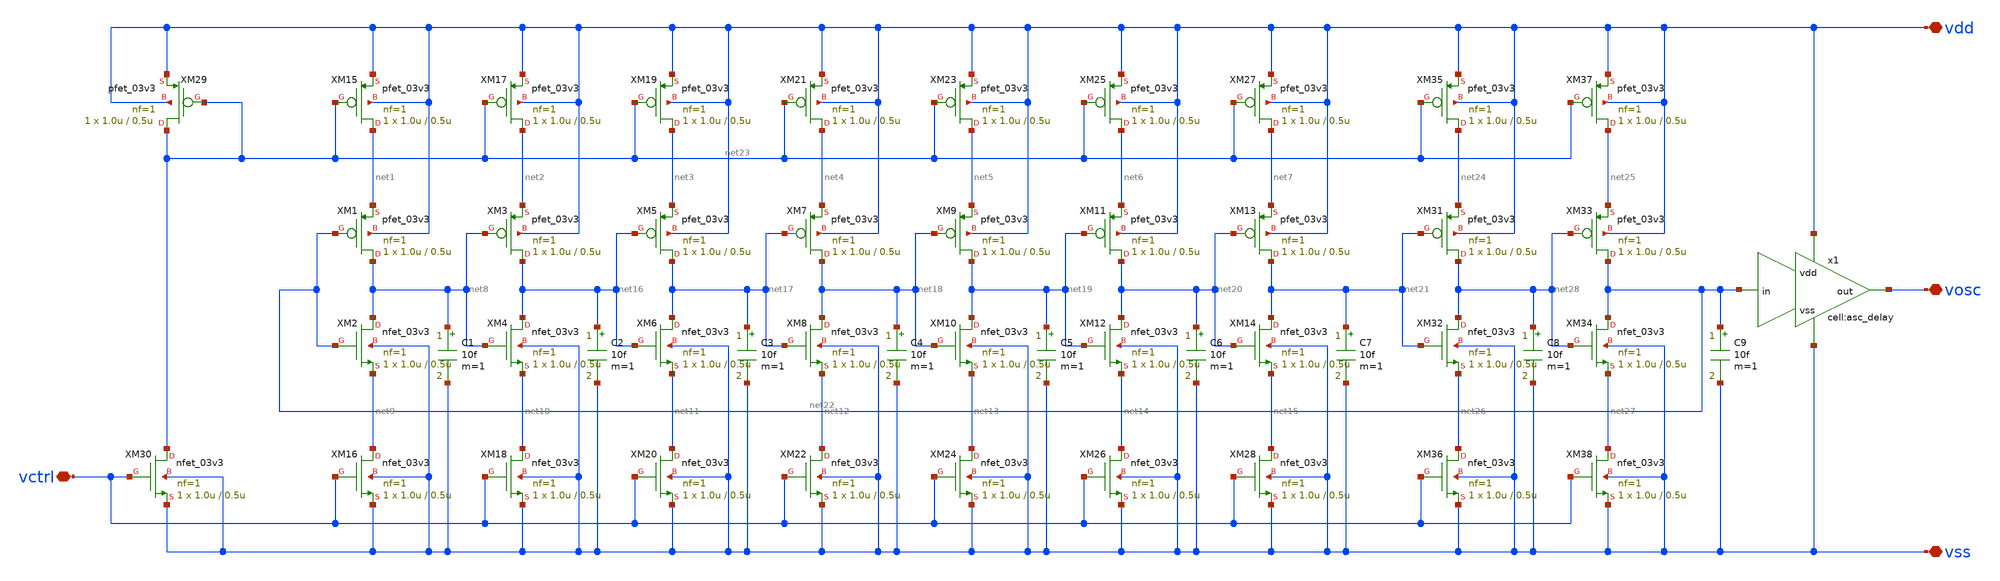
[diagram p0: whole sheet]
** sch_path: designs/libs/core_analog/CSRVCO_20250818/CSRVCO_20250818.sch
**.subckt CSRVCO_20250818 vdd vss vosc vctrl
*.iopin vdd
*.iopin vss
*.iopin vosc
*.iopin vctrl
XM1 net8 net22 net1 vdd pfet_03v3 L=0.5u W=1.0u nf=1 ad='int((nf+1)/2) * W/nf * 0.18u' as='int((nf+2)/2) * W/nf * 0.18u'
+ pd='2*int((nf+1)/2) * (W/nf + 0.18u)' ps='2*int((nf+2)/2) * (W/nf + 0.18u)' nrd='0.18u / W' nrs='0.18u / W'
+ sa=0 sb=0 sd=0 m=1
XM2 net8 net22 net9 vss nfet_03v3 L=0.5u W=1.0u nf=1 ad='int((nf+1)/2) * W/nf * 0.18u' as='int((nf+2)/2) * W/nf * 0.18u'
+ pd='2*int((nf+1)/2) * (W/nf + 0.18u)' ps='2*int((nf+2)/2) * (W/nf + 0.18u)' nrd='0.18u / W' nrs='0.18u / W'
+ sa=0 sb=0 sd=0 m=1
XM3 net16 net8 net2 vdd pfet_03v3 L=0.5u W=1.0u nf=1 ad='int((nf+1)/2) * W/nf * 0.18u' as='int((nf+2)/2) * W/nf * 0.18u'
+ pd='2*int((nf+1)/2) * (W/nf + 0.18u)' ps='2*int((nf+2)/2) * (W/nf + 0.18u)' nrd='0.18u / W' nrs='0.18u / W'
+ sa=0 sb=0 sd=0 m=1
XM4 net16 net8 net10 vss nfet_03v3 L=0.5u W=1.0u nf=1 ad='int((nf+1)/2) * W/nf * 0.18u' as='int((nf+2)/2) * W/nf * 0.18u'
+ pd='2*int((nf+1)/2) * (W/nf + 0.18u)' ps='2*int((nf+2)/2) * (W/nf + 0.18u)' nrd='0.18u / W' nrs='0.18u / W'
+ sa=0 sb=0 sd=0 m=1
XM5 net17 net16 net3 vdd pfet_03v3 L=0.5u W=1.0u nf=1 ad='int((nf+1)/2) * W/nf * 0.18u' as='int((nf+2)/2) * W/nf * 0.18u'
+ pd='2*int((nf+1)/2) * (W/nf + 0.18u)' ps='2*int((nf+2)/2) * (W/nf + 0.18u)' nrd='0.18u / W' nrs='0.18u / W'
+ sa=0 sb=0 sd=0 m=1
XM6 net17 net16 net11 vss nfet_03v3 L=0.5u W=1.0u nf=1 ad='int((nf+1)/2) * W/nf * 0.18u' as='int((nf+2)/2) * W/nf * 0.18u'
+ pd='2*int((nf+1)/2) * (W/nf + 0.18u)' ps='2*int((nf+2)/2) * (W/nf + 0.18u)' nrd='0.18u / W' nrs='0.18u / W'
+ sa=0 sb=0 sd=0 m=1
XM7 net18 net17 net4 vdd pfet_03v3 L=0.5u W=1.0u nf=1 ad='int((nf+1)/2) * W/nf * 0.18u' as='int((nf+2)/2) * W/nf * 0.18u'
+ pd='2*int((nf+1)/2) * (W/nf + 0.18u)' ps='2*int((nf+2)/2) * (W/nf + 0.18u)' nrd='0.18u / W' nrs='0.18u / W'
+ sa=0 sb=0 sd=0 m=1
XM8 net18 net17 net12 vss nfet_03v3 L=0.5u W=1.0u nf=1 ad='int((nf+1)/2) * W/nf * 0.18u' as='int((nf+2)/2) * W/nf * 0.18u'
+ pd='2*int((nf+1)/2) * (W/nf + 0.18u)' ps='2*int((nf+2)/2) * (W/nf + 0.18u)' nrd='0.18u / W' nrs='0.18u / W'
+ sa=0 sb=0 sd=0 m=1
XM9 net19 net18 net5 vdd pfet_03v3 L=0.5u W=1.0u nf=1 ad='int((nf+1)/2) * W/nf * 0.18u' as='int((nf+2)/2) * W/nf * 0.18u'
+ pd='2*int((nf+1)/2) * (W/nf + 0.18u)' ps='2*int((nf+2)/2) * (W/nf + 0.18u)' nrd='0.18u / W' nrs='0.18u / W'
+ sa=0 sb=0 sd=0 m=1
XM10 net19 net18 net13 vss nfet_03v3 L=0.5u W=1.0u nf=1 ad='int((nf+1)/2) * W/nf * 0.18u' as='int((nf+2)/2) * W/nf * 0.18u'
+ pd='2*int((nf+1)/2) * (W/nf + 0.18u)' ps='2*int((nf+2)/2) * (W/nf + 0.18u)' nrd='0.18u / W' nrs='0.18u / W'
+ sa=0 sb=0 sd=0 m=1
XM11 net20 net19 net6 vdd pfet_03v3 L=0.5u W=1.0u nf=1 ad='int((nf+1)/2) * W/nf * 0.18u' as='int((nf+2)/2) * W/nf * 0.18u'
+ pd='2*int((nf+1)/2) * (W/nf + 0.18u)' ps='2*int((nf+2)/2) * (W/nf + 0.18u)' nrd='0.18u / W' nrs='0.18u / W'
+ sa=0 sb=0 sd=0 m=1
XM12 net20 net19 net14 vss nfet_03v3 L=0.5u W=1.0u nf=1 ad='int((nf+1)/2) * W/nf * 0.18u' as='int((nf+2)/2) * W/nf * 0.18u'
+ pd='2*int((nf+1)/2) * (W/nf + 0.18u)' ps='2*int((nf+2)/2) * (W/nf + 0.18u)' nrd='0.18u / W' nrs='0.18u / W'
+ sa=0 sb=0 sd=0 m=1
XM13 net21 net20 net7 vdd pfet_03v3 L=0.5u W=1.0u nf=1 ad='int((nf+1)/2) * W/nf * 0.18u' as='int((nf+2)/2) * W/nf * 0.18u'
+ pd='2*int((nf+1)/2) * (W/nf + 0.18u)' ps='2*int((nf+2)/2) * (W/nf + 0.18u)' nrd='0.18u / W' nrs='0.18u / W'
+ sa=0 sb=0 sd=0 m=1
XM14 net21 net20 net15 vss nfet_03v3 L=0.5u W=1.0u nf=1 ad='int((nf+1)/2) * W/nf * 0.18u' as='int((nf+2)/2) * W/nf * 0.18u'
+ pd='2*int((nf+1)/2) * (W/nf + 0.18u)' ps='2*int((nf+2)/2) * (W/nf + 0.18u)' nrd='0.18u / W' nrs='0.18u / W'
+ sa=0 sb=0 sd=0 m=1
XM15 net1 net23 vdd vdd pfet_03v3 L=0.5u W=1.0u nf=1 ad='int((nf+1)/2) * W/nf * 0.18u' as='int((nf+2)/2) * W/nf * 0.18u'
+ pd='2*int((nf+1)/2) * (W/nf + 0.18u)' ps='2*int((nf+2)/2) * (W/nf + 0.18u)' nrd='0.18u / W' nrs='0.18u / W'
+ sa=0 sb=0 sd=0 m=1
XM16 net9 vctrl vss vss nfet_03v3 L=0.5u W=1.0u nf=1 ad='int((nf+1)/2) * W/nf * 0.18u' as='int((nf+2)/2) * W/nf * 0.18u'
+ pd='2*int((nf+1)/2) * (W/nf + 0.18u)' ps='2*int((nf+2)/2) * (W/nf + 0.18u)' nrd='0.18u / W' nrs='0.18u / W'
+ sa=0 sb=0 sd=0 m=1
XM17 net2 net23 vdd vdd pfet_03v3 L=0.5u W=1.0u nf=1 ad='int((nf+1)/2) * W/nf * 0.18u' as='int((nf+2)/2) * W/nf * 0.18u'
+ pd='2*int((nf+1)/2) * (W/nf + 0.18u)' ps='2*int((nf+2)/2) * (W/nf + 0.18u)' nrd='0.18u / W' nrs='0.18u / W'
+ sa=0 sb=0 sd=0 m=1
XM18 net10 vctrl vss vss nfet_03v3 L=0.5u W=1.0u nf=1 ad='int((nf+1)/2) * W/nf * 0.18u' as='int((nf+2)/2) * W/nf * 0.18u'
+ pd='2*int((nf+1)/2) * (W/nf + 0.18u)' ps='2*int((nf+2)/2) * (W/nf + 0.18u)' nrd='0.18u / W' nrs='0.18u / W'
+ sa=0 sb=0 sd=0 m=1
XM19 net3 net23 vdd vdd pfet_03v3 L=0.5u W=1.0u nf=1 ad='int((nf+1)/2) * W/nf * 0.18u' as='int((nf+2)/2) * W/nf * 0.18u'
+ pd='2*int((nf+1)/2) * (W/nf + 0.18u)' ps='2*int((nf+2)/2) * (W/nf + 0.18u)' nrd='0.18u / W' nrs='0.18u / W'
+ sa=0 sb=0 sd=0 m=1
XM20 net11 vctrl vss vss nfet_03v3 L=0.5u W=1.0u nf=1 ad='int((nf+1)/2) * W/nf * 0.18u' as='int((nf+2)/2) * W/nf * 0.18u'
+ pd='2*int((nf+1)/2) * (W/nf + 0.18u)' ps='2*int((nf+2)/2) * (W/nf + 0.18u)' nrd='0.18u / W' nrs='0.18u / W'
+ sa=0 sb=0 sd=0 m=1
XM21 net4 net23 vdd vdd pfet_03v3 L=0.5u W=1.0u nf=1 ad='int((nf+1)/2) * W/nf * 0.18u' as='int((nf+2)/2) * W/nf * 0.18u'
+ pd='2*int((nf+1)/2) * (W/nf + 0.18u)' ps='2*int((nf+2)/2) * (W/nf + 0.18u)' nrd='0.18u / W' nrs='0.18u / W'
+ sa=0 sb=0 sd=0 m=1
XM22 net12 vctrl vss vss nfet_03v3 L=0.5u W=1.0u nf=1 ad='int((nf+1)/2) * W/nf * 0.18u' as='int((nf+2)/2) * W/nf * 0.18u'
+ pd='2*int((nf+1)/2) * (W/nf + 0.18u)' ps='2*int((nf+2)/2) * (W/nf + 0.18u)' nrd='0.18u / W' nrs='0.18u / W'
+ sa=0 sb=0 sd=0 m=1
XM23 net5 net23 vdd vdd pfet_03v3 L=0.5u W=1.0u nf=1 ad='int((nf+1)/2) * W/nf * 0.18u' as='int((nf+2)/2) * W/nf * 0.18u'
+ pd='2*int((nf+1)/2) * (W/nf + 0.18u)' ps='2*int((nf+2)/2) * (W/nf + 0.18u)' nrd='0.18u / W' nrs='0.18u / W'
+ sa=0 sb=0 sd=0 m=1
XM24 net13 vctrl vss vss nfet_03v3 L=0.5u W=1.0u nf=1 ad='int((nf+1)/2) * W/nf * 0.18u' as='int((nf+2)/2) * W/nf * 0.18u'
+ pd='2*int((nf+1)/2) * (W/nf + 0.18u)' ps='2*int((nf+2)/2) * (W/nf + 0.18u)' nrd='0.18u / W' nrs='0.18u / W'
+ sa=0 sb=0 sd=0 m=1
XM25 net6 net23 vdd vdd pfet_03v3 L=0.5u W=1.0u nf=1 ad='int((nf+1)/2) * W/nf * 0.18u' as='int((nf+2)/2) * W/nf * 0.18u'
+ pd='2*int((nf+1)/2) * (W/nf + 0.18u)' ps='2*int((nf+2)/2) * (W/nf + 0.18u)' nrd='0.18u / W' nrs='0.18u / W'
+ sa=0 sb=0 sd=0 m=1
XM26 net14 vctrl vss vss nfet_03v3 L=0.5u W=1.0u nf=1 ad='int((nf+1)/2) * W/nf * 0.18u' as='int((nf+2)/2) * W/nf * 0.18u'
+ pd='2*int((nf+1)/2) * (W/nf + 0.18u)' ps='2*int((nf+2)/2) * (W/nf + 0.18u)' nrd='0.18u / W' nrs='0.18u / W'
+ sa=0 sb=0 sd=0 m=1
XM27 net7 net23 vdd vdd pfet_03v3 L=0.5u W=1.0u nf=1 ad='int((nf+1)/2) * W/nf * 0.18u' as='int((nf+2)/2) * W/nf * 0.18u'
+ pd='2*int((nf+1)/2) * (W/nf + 0.18u)' ps='2*int((nf+2)/2) * (W/nf + 0.18u)' nrd='0.18u / W' nrs='0.18u / W'
+ sa=0 sb=0 sd=0 m=1
XM28 net15 vctrl vss vss nfet_03v3 L=0.5u W=1.0u nf=1 ad='int((nf+1)/2) * W/nf * 0.18u' as='int((nf+2)/2) * W/nf * 0.18u'
+ pd='2*int((nf+1)/2) * (W/nf + 0.18u)' ps='2*int((nf+2)/2) * (W/nf + 0.18u)' nrd='0.18u / W' nrs='0.18u / W'
+ sa=0 sb=0 sd=0 m=1
XM29 net23 net23 vdd vdd pfet_03v3 L=0.5u W=1.0u nf=1 ad='int((nf+1)/2) * W/nf * 0.18u' as='int((nf+2)/2) * W/nf * 0.18u'
+ pd='2*int((nf+1)/2) * (W/nf + 0.18u)' ps='2*int((nf+2)/2) * (W/nf + 0.18u)' nrd='0.18u / W' nrs='0.18u / W'
+ sa=0 sb=0 sd=0 m=1
XM30 net23 vctrl vss vss nfet_03v3 L=0.5u W=1.0u nf=1 ad='int((nf+1)/2) * W/nf * 0.18u' as='int((nf+2)/2) * W/nf * 0.18u'
+ pd='2*int((nf+1)/2) * (W/nf + 0.18u)' ps='2*int((nf+2)/2) * (W/nf + 0.18u)' nrd='0.18u / W' nrs='0.18u / W'
+ sa=0 sb=0 sd=0 m=1
x1 net22 vss vosc vdd asc_delay
XM31 net28 net21 net24 vdd pfet_03v3 L=0.5u W=1.0u nf=1 ad='int((nf+1)/2) * W/nf * 0.18u' as='int((nf+2)/2) * W/nf * 0.18u'
+ pd='2*int((nf+1)/2) * (W/nf + 0.18u)' ps='2*int((nf+2)/2) * (W/nf + 0.18u)' nrd='0.18u / W' nrs='0.18u / W'
+ sa=0 sb=0 sd=0 m=1
XM32 net28 net21 net26 vss nfet_03v3 L=0.5u W=1.0u nf=1 ad='int((nf+1)/2) * W/nf * 0.18u' as='int((nf+2)/2) * W/nf * 0.18u'
+ pd='2*int((nf+1)/2) * (W/nf + 0.18u)' ps='2*int((nf+2)/2) * (W/nf + 0.18u)' nrd='0.18u / W' nrs='0.18u / W'
+ sa=0 sb=0 sd=0 m=1
XM33 net22 net28 net25 vdd pfet_03v3 L=0.5u W=1.0u nf=1 ad='int((nf+1)/2) * W/nf * 0.18u' as='int((nf+2)/2) * W/nf * 0.18u'
+ pd='2*int((nf+1)/2) * (W/nf + 0.18u)' ps='2*int((nf+2)/2) * (W/nf + 0.18u)' nrd='0.18u / W' nrs='0.18u / W'
+ sa=0 sb=0 sd=0 m=1
XM34 net22 net28 net27 vss nfet_03v3 L=0.5u W=1.0u nf=1 ad='int((nf+1)/2) * W/nf * 0.18u' as='int((nf+2)/2) * W/nf * 0.18u'
+ pd='2*int((nf+1)/2) * (W/nf + 0.18u)' ps='2*int((nf+2)/2) * (W/nf + 0.18u)' nrd='0.18u / W' nrs='0.18u / W'
+ sa=0 sb=0 sd=0 m=1
XM35 net24 net23 vdd vdd pfet_03v3 L=0.5u W=1.0u nf=1 ad='int((nf+1)/2) * W/nf * 0.18u' as='int((nf+2)/2) * W/nf * 0.18u'
+ pd='2*int((nf+1)/2) * (W/nf + 0.18u)' ps='2*int((nf+2)/2) * (W/nf + 0.18u)' nrd='0.18u / W' nrs='0.18u / W'
+ sa=0 sb=0 sd=0 m=1
XM36 net26 vctrl vss vss nfet_03v3 L=0.5u W=1.0u nf=1 ad='int((nf+1)/2) * W/nf * 0.18u' as='int((nf+2)/2) * W/nf * 0.18u'
+ pd='2*int((nf+1)/2) * (W/nf + 0.18u)' ps='2*int((nf+2)/2) * (W/nf + 0.18u)' nrd='0.18u / W' nrs='0.18u / W'
+ sa=0 sb=0 sd=0 m=1
XM37 net25 net23 vdd vdd pfet_03v3 L=0.5u W=1.0u nf=1 ad='int((nf+1)/2) * W/nf * 0.18u' as='int((nf+2)/2) * W/nf * 0.18u'
+ pd='2*int((nf+1)/2) * (W/nf + 0.18u)' ps='2*int((nf+2)/2) * (W/nf + 0.18u)' nrd='0.18u / W' nrs='0.18u / W'
+ sa=0 sb=0 sd=0 m=1
XM38 net27 vctrl vss vss nfet_03v3 L=0.5u W=1.0u nf=1 ad='int((nf+1)/2) * W/nf * 0.18u' as='int((nf+2)/2) * W/nf * 0.18u'
+ pd='2*int((nf+1)/2) * (W/nf + 0.18u)' ps='2*int((nf+2)/2) * (W/nf + 0.18u)' nrd='0.18u / W' nrs='0.18u / W'
+ sa=0 sb=0 sd=0 m=1
C1 net8 vss 10f m=1
C2 net16 vss 10f m=1
C3 net17 vss 10f m=1
C4 net18 vss 10f m=1
C5 net19 vss 10f m=1
C6 net20 vss 10f m=1
C7 net21 vss 10f m=1
C8 net28 vss 10f m=1
C9 net22 vss 10f m=1
**.ends
.end
